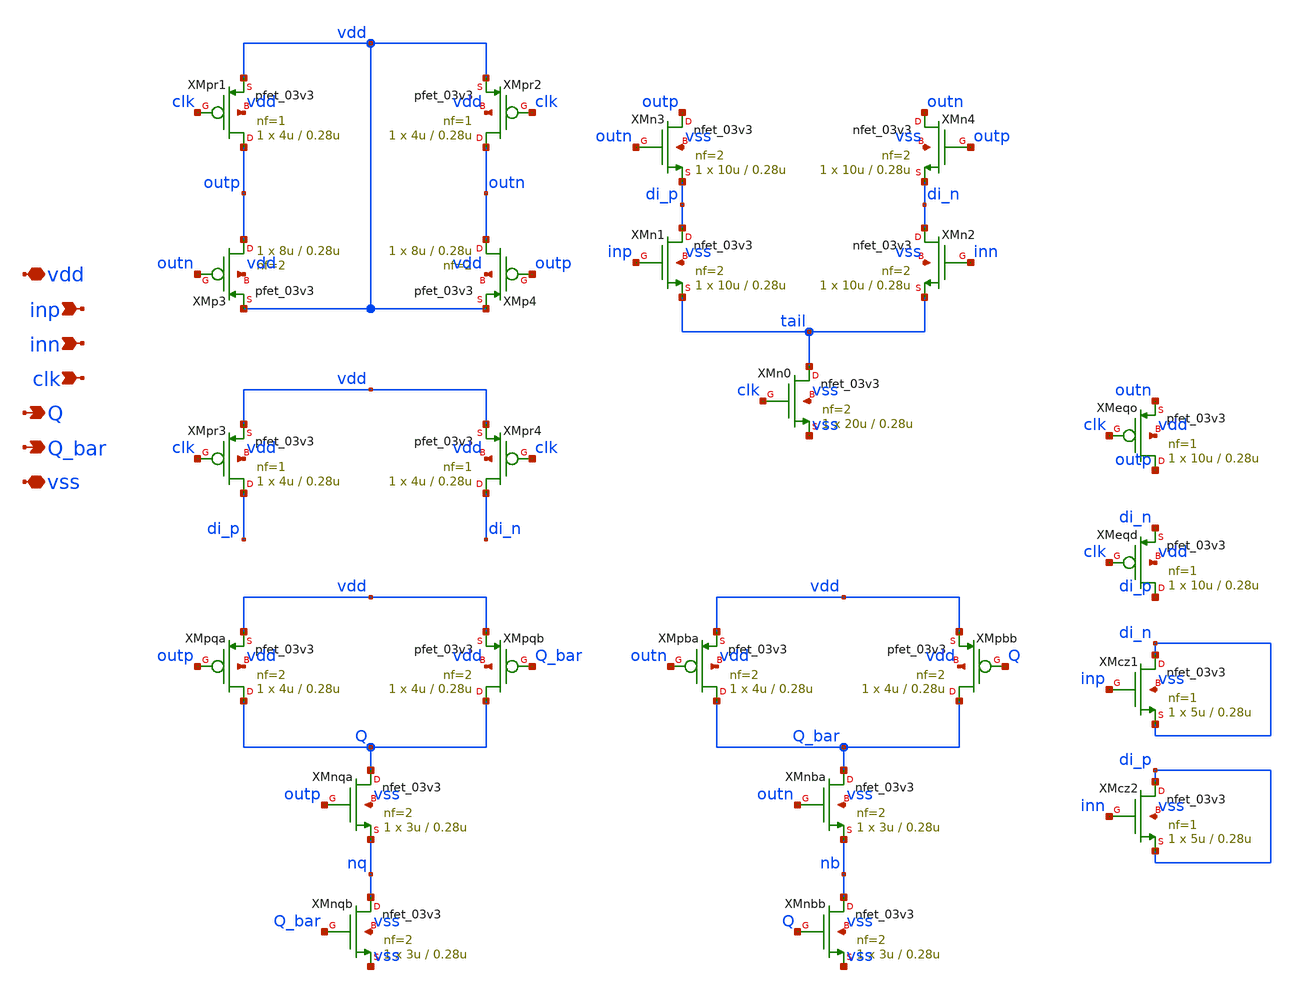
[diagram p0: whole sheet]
** sch_path: blocks/adc/comp-array/compact/strongarm.sch
**.subckt strongarm vdd inp inn clk Q Q_bar vss
*.iopin vdd
*.ipin inp
*.ipin inn
*.ipin clk
*.opin Q
*.opin Q_bar
*.iopin vss
XMpr1 outp clk vdd vdd pfet_03v3 L=0.28u W=4u nf=1 ad='int((nf+1)/2) * W/nf * 0.18u' as='int((nf+2)/2) * W/nf * 0.18u'
+ pd='2*int((nf+1)/2) * (W/nf + 0.18u)' ps='2*int((nf+2)/2) * (W/nf + 0.18u)' nrd='0.18u / W' nrs='0.18u / W'
+ sa=0 sb=0 sd=0 m=1
XMpr2 outn clk vdd vdd pfet_03v3 L=0.28u W=4u nf=1 ad='int((nf+1)/2) * W/nf * 0.18u' as='int((nf+2)/2) * W/nf * 0.18u'
+ pd='2*int((nf+1)/2) * (W/nf + 0.18u)' ps='2*int((nf+2)/2) * (W/nf + 0.18u)' nrd='0.18u / W' nrs='0.18u / W'
+ sa=0 sb=0 sd=0 m=1
XMp3 outp outn vdd vdd pfet_03v3 L=0.28u W=8u nf=2 ad='int((nf+1)/2) * W/nf * 0.18u' as='int((nf+2)/2) * W/nf * 0.18u'
+ pd='2*int((nf+1)/2) * (W/nf + 0.18u)' ps='2*int((nf+2)/2) * (W/nf + 0.18u)' nrd='0.18u / W' nrs='0.18u / W'
+ sa=0 sb=0 sd=0 m=1
XMp4 outn outp vdd vdd pfet_03v3 L=0.28u W=8u nf=2 ad='int((nf+1)/2) * W/nf * 0.18u' as='int((nf+2)/2) * W/nf * 0.18u'
+ pd='2*int((nf+1)/2) * (W/nf + 0.18u)' ps='2*int((nf+2)/2) * (W/nf + 0.18u)' nrd='0.18u / W' nrs='0.18u / W'
+ sa=0 sb=0 sd=0 m=1
XMn3 outp outn di_p vss nfet_03v3 L=0.28u W=10u nf=2 ad='int((nf+1)/2) * W/nf * 0.18u' as='int((nf+2)/2) * W/nf * 0.18u'
+ pd='2*int((nf+1)/2) * (W/nf + 0.18u)' ps='2*int((nf+2)/2) * (W/nf + 0.18u)' nrd='0.18u / W' nrs='0.18u / W'
+ sa=0 sb=0 sd=0 m=1
XMn4 outn outp di_n vss nfet_03v3 L=0.28u W=10u nf=2 ad='int((nf+1)/2) * W/nf * 0.18u' as='int((nf+2)/2) * W/nf * 0.18u'
+ pd='2*int((nf+1)/2) * (W/nf + 0.18u)' ps='2*int((nf+2)/2) * (W/nf + 0.18u)' nrd='0.18u / W' nrs='0.18u / W'
+ sa=0 sb=0 sd=0 m=1
XMn1 di_p inp tail vss nfet_03v3 L=0.28u W=10u nf=2 ad='int((nf+1)/2) * W/nf * 0.18u' as='int((nf+2)/2) * W/nf * 0.18u'
+ pd='2*int((nf+1)/2) * (W/nf + 0.18u)' ps='2*int((nf+2)/2) * (W/nf + 0.18u)' nrd='0.18u / W' nrs='0.18u / W'
+ sa=0 sb=0 sd=0 m=1
XMn2 di_n inn tail vss nfet_03v3 L=0.28u W=10u nf=2 ad='int((nf+1)/2) * W/nf * 0.18u' as='int((nf+2)/2) * W/nf * 0.18u'
+ pd='2*int((nf+1)/2) * (W/nf + 0.18u)' ps='2*int((nf+2)/2) * (W/nf + 0.18u)' nrd='0.18u / W' nrs='0.18u / W'
+ sa=0 sb=0 sd=0 m=1
XMn0 tail clk vss vss nfet_03v3 L=0.28u W=20u nf=2 ad='int((nf+1)/2) * W/nf * 0.18u' as='int((nf+2)/2) * W/nf * 0.18u'
+ pd='2*int((nf+1)/2) * (W/nf + 0.18u)' ps='2*int((nf+2)/2) * (W/nf + 0.18u)' nrd='0.18u / W' nrs='0.18u / W'
+ sa=0 sb=0 sd=0 m=1
XMpr3 di_p clk vdd vdd pfet_03v3 L=0.28u W=4u nf=1 ad='int((nf+1)/2) * W/nf * 0.18u' as='int((nf+2)/2) * W/nf * 0.18u'
+ pd='2*int((nf+1)/2) * (W/nf + 0.18u)' ps='2*int((nf+2)/2) * (W/nf + 0.18u)' nrd='0.18u / W' nrs='0.18u / W'
+ sa=0 sb=0 sd=0 m=1
XMpr4 di_n clk vdd vdd pfet_03v3 L=0.28u W=4u nf=1 ad='int((nf+1)/2) * W/nf * 0.18u' as='int((nf+2)/2) * W/nf * 0.18u'
+ pd='2*int((nf+1)/2) * (W/nf + 0.18u)' ps='2*int((nf+2)/2) * (W/nf + 0.18u)' nrd='0.18u / W' nrs='0.18u / W'
+ sa=0 sb=0 sd=0 m=1
XMpqa Q outp vdd vdd pfet_03v3 L=0.28u W=4u nf=2 ad='int((nf+1)/2) * W/nf * 0.18u' as='int((nf+2)/2) * W/nf * 0.18u'
+ pd='2*int((nf+1)/2) * (W/nf + 0.18u)' ps='2*int((nf+2)/2) * (W/nf + 0.18u)' nrd='0.18u / W' nrs='0.18u / W'
+ sa=0 sb=0 sd=0 m=1
XMpqb Q Q_bar vdd vdd pfet_03v3 L=0.28u W=4u nf=2 ad='int((nf+1)/2) * W/nf * 0.18u' as='int((nf+2)/2) * W/nf * 0.18u'
+ pd='2*int((nf+1)/2) * (W/nf + 0.18u)' ps='2*int((nf+2)/2) * (W/nf + 0.18u)' nrd='0.18u / W' nrs='0.18u / W'
+ sa=0 sb=0 sd=0 m=1
XMnqa Q outp nq vss nfet_03v3 L=0.28u W=3u nf=2 ad='int((nf+1)/2) * W/nf * 0.18u' as='int((nf+2)/2) * W/nf * 0.18u'
+ pd='2*int((nf+1)/2) * (W/nf + 0.18u)' ps='2*int((nf+2)/2) * (W/nf + 0.18u)' nrd='0.18u / W' nrs='0.18u / W'
+ sa=0 sb=0 sd=0 m=1
XMnqb nq Q_bar vss vss nfet_03v3 L=0.28u W=3u nf=2 ad='int((nf+1)/2) * W/nf * 0.18u' as='int((nf+2)/2) * W/nf * 0.18u'
+ pd='2*int((nf+1)/2) * (W/nf + 0.18u)' ps='2*int((nf+2)/2) * (W/nf + 0.18u)' nrd='0.18u / W' nrs='0.18u / W'
+ sa=0 sb=0 sd=0 m=1
XMpba Q_bar outn vdd vdd pfet_03v3 L=0.28u W=4u nf=2 ad='int((nf+1)/2) * W/nf * 0.18u' as='int((nf+2)/2) * W/nf * 0.18u'
+ pd='2*int((nf+1)/2) * (W/nf + 0.18u)' ps='2*int((nf+2)/2) * (W/nf + 0.18u)' nrd='0.18u / W' nrs='0.18u / W'
+ sa=0 sb=0 sd=0 m=1
XMpbb Q_bar Q vdd vdd pfet_03v3 L=0.28u W=4u nf=2 ad='int((nf+1)/2) * W/nf * 0.18u' as='int((nf+2)/2) * W/nf * 0.18u'
+ pd='2*int((nf+1)/2) * (W/nf + 0.18u)' ps='2*int((nf+2)/2) * (W/nf + 0.18u)' nrd='0.18u / W' nrs='0.18u / W'
+ sa=0 sb=0 sd=0 m=1
XMnba Q_bar outn nb vss nfet_03v3 L=0.28u W=3u nf=2 ad='int((nf+1)/2) * W/nf * 0.18u' as='int((nf+2)/2) * W/nf * 0.18u'
+ pd='2*int((nf+1)/2) * (W/nf + 0.18u)' ps='2*int((nf+2)/2) * (W/nf + 0.18u)' nrd='0.18u / W' nrs='0.18u / W'
+ sa=0 sb=0 sd=0 m=1
XMnbb nb Q vss vss nfet_03v3 L=0.28u W=3u nf=2 ad='int((nf+1)/2) * W/nf * 0.18u' as='int((nf+2)/2) * W/nf * 0.18u'
+ pd='2*int((nf+1)/2) * (W/nf + 0.18u)' ps='2*int((nf+2)/2) * (W/nf + 0.18u)' nrd='0.18u / W' nrs='0.18u / W'
+ sa=0 sb=0 sd=0 m=1
XMeqo outp clk outn vdd pfet_03v3 L=0.28u W=10u nf=1 ad='int((nf+1)/2) * W/nf * 0.18u' as='int((nf+2)/2) * W/nf * 0.18u'
+ pd='2*int((nf+1)/2) * (W/nf + 0.18u)' ps='2*int((nf+2)/2) * (W/nf + 0.18u)' nrd='0.18u / W' nrs='0.18u / W'
+ sa=0 sb=0 sd=0 m=1
XMeqd di_p clk di_n vdd pfet_03v3 L=0.28u W=10u nf=1 ad='int((nf+1)/2) * W/nf * 0.18u' as='int((nf+2)/2) * W/nf * 0.18u'
+ pd='2*int((nf+1)/2) * (W/nf + 0.18u)' ps='2*int((nf+2)/2) * (W/nf + 0.18u)' nrd='0.18u / W' nrs='0.18u / W'
+ sa=0 sb=0 sd=0 m=1
XMcz1 di_n inp di_n vss nfet_03v3 L=0.28u W=5u nf=1 ad='int((nf+1)/2) * W/nf * 0.18u' as='int((nf+2)/2) * W/nf * 0.18u'
+ pd='2*int((nf+1)/2) * (W/nf + 0.18u)' ps='2*int((nf+2)/2) * (W/nf + 0.18u)' nrd='0.18u / W' nrs='0.18u / W'
+ sa=0 sb=0 sd=0 m=1
XMcz2 di_p inn di_p vss nfet_03v3 L=0.28u W=5u nf=1 ad='int((nf+1)/2) * W/nf * 0.18u' as='int((nf+2)/2) * W/nf * 0.18u'
+ pd='2*int((nf+1)/2) * (W/nf + 0.18u)' ps='2*int((nf+2)/2) * (W/nf + 0.18u)' nrd='0.18u / W' nrs='0.18u / W'
+ sa=0 sb=0 sd=0 m=1
**.ends
.end
